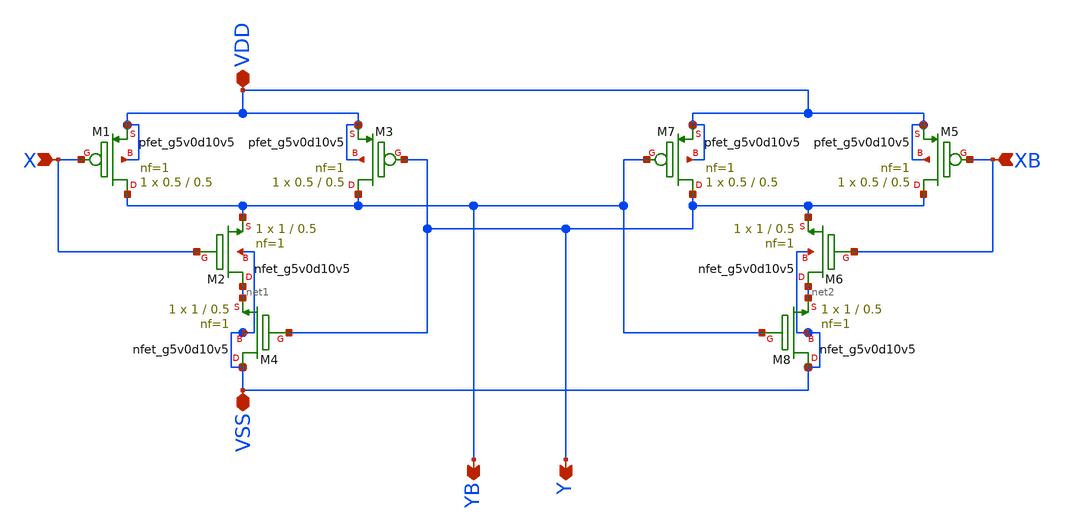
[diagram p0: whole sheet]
** sch_path: xschem/clock_3v3/nonoverlapping_generator.sch
**.subckt nonoverlapping_generator VSS VDD X XB YB Y
*.iopin VSS
*.iopin VDD
*.ipin X
*.ipin XB
*.opin YB
*.opin Y
XM1 YB X VDD VDD sky130_fd_pr__pfet_g5v0d10v5 L=0.5 W=0.5 nf=1 ad='int((nf+1)/2) * W/nf * 0.29' as='int((nf+2)/2) * W/nf * 0.29'
+ pd='2*int((nf+1)/2) * (W/nf + 0.29)' ps='2*int((nf+2)/2) * (W/nf + 0.29)' nrd='0.29 / W' nrs='0.29 / W'
+ sa=0 sb=0 sd=0 mult=1 m=1
XM2 net1 X YB VSS sky130_fd_pr__nfet_g5v0d10v5 L=0.5 W=1 nf=1 ad='int((nf+1)/2) * W/nf * 0.29' as='int((nf+2)/2) * W/nf * 0.29'
+ pd='2*int((nf+1)/2) * (W/nf + 0.29)' ps='2*int((nf+2)/2) * (W/nf + 0.29)' nrd='0.29 / W' nrs='0.29 / W'
+ sa=0 sb=0 sd=0 mult=1 m=1
XM3 YB Y VDD VDD sky130_fd_pr__pfet_g5v0d10v5 L=0.5 W=0.5 nf=1 ad='int((nf+1)/2) * W/nf * 0.29' as='int((nf+2)/2) * W/nf * 0.29'
+ pd='2*int((nf+1)/2) * (W/nf + 0.29)' ps='2*int((nf+2)/2) * (W/nf + 0.29)' nrd='0.29 / W' nrs='0.29 / W'
+ sa=0 sb=0 sd=0 mult=1 m=1
XM4 VSS Y net1 VSS sky130_fd_pr__nfet_g5v0d10v5 L=0.5 W=1 nf=1 ad='int((nf+1)/2) * W/nf * 0.29' as='int((nf+2)/2) * W/nf * 0.29'
+ pd='2*int((nf+1)/2) * (W/nf + 0.29)' ps='2*int((nf+2)/2) * (W/nf + 0.29)' nrd='0.29 / W' nrs='0.29 / W'
+ sa=0 sb=0 sd=0 mult=1 m=1
XM5 Y XB VDD VDD sky130_fd_pr__pfet_g5v0d10v5 L=0.5 W=0.5 nf=1 ad='int((nf+1)/2) * W/nf * 0.29' as='int((nf+2)/2) * W/nf * 0.29'
+ pd='2*int((nf+1)/2) * (W/nf + 0.29)' ps='2*int((nf+2)/2) * (W/nf + 0.29)' nrd='0.29 / W' nrs='0.29 / W'
+ sa=0 sb=0 sd=0 mult=1 m=1
XM6 net2 XB Y VSS sky130_fd_pr__nfet_g5v0d10v5 L=0.5 W=1 nf=1 ad='int((nf+1)/2) * W/nf * 0.29' as='int((nf+2)/2) * W/nf * 0.29'
+ pd='2*int((nf+1)/2) * (W/nf + 0.29)' ps='2*int((nf+2)/2) * (W/nf + 0.29)' nrd='0.29 / W' nrs='0.29 / W'
+ sa=0 sb=0 sd=0 mult=1 m=1
XM7 Y YB VDD VDD sky130_fd_pr__pfet_g5v0d10v5 L=0.5 W=0.5 nf=1 ad='int((nf+1)/2) * W/nf * 0.29' as='int((nf+2)/2) * W/nf * 0.29'
+ pd='2*int((nf+1)/2) * (W/nf + 0.29)' ps='2*int((nf+2)/2) * (W/nf + 0.29)' nrd='0.29 / W' nrs='0.29 / W'
+ sa=0 sb=0 sd=0 mult=1 m=1
XM8 VSS YB net2 VSS sky130_fd_pr__nfet_g5v0d10v5 L=0.5 W=1 nf=1 ad='int((nf+1)/2) * W/nf * 0.29' as='int((nf+2)/2) * W/nf * 0.29'
+ pd='2*int((nf+1)/2) * (W/nf + 0.29)' ps='2*int((nf+2)/2) * (W/nf + 0.29)' nrd='0.29 / W' nrs='0.29 / W'
+ sa=0 sb=0 sd=0 mult=1 m=1
**.ends
.end
